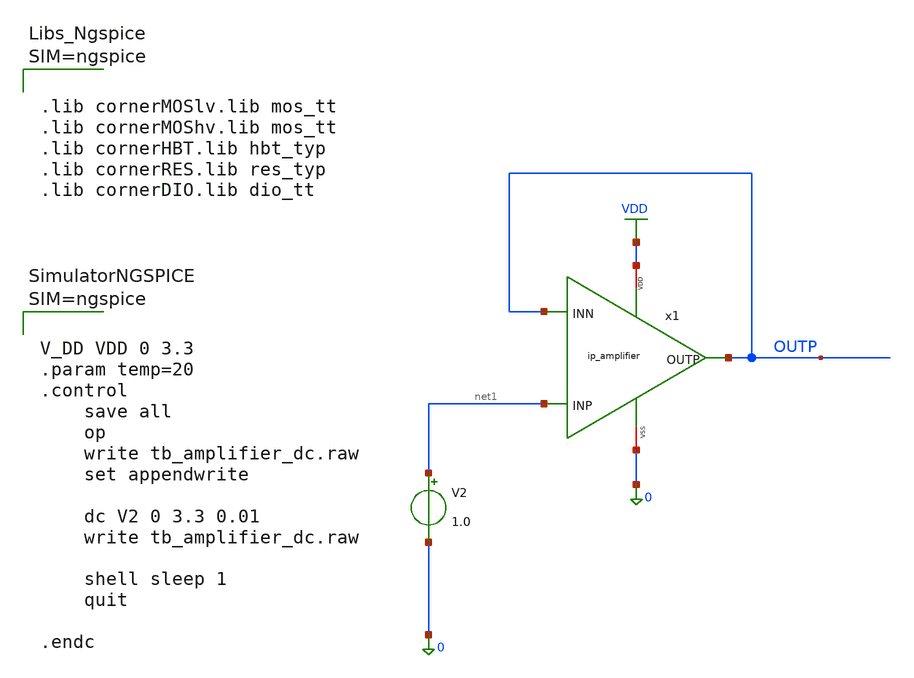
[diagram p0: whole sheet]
** sch_path: xschem/tb_amplifier_dc.sch
**.subckt tb_amplifier_dc
x1 VDD OUTP OUTP net1 0 ip_amplifier
V2 net1 0 1.0
**** begin user architecture code



.lib cornerMOSlv.lib mos_tt
.lib cornerMOShv.lib mos_tt
.lib cornerHBT.lib hbt_typ
.lib cornerRES.lib res_typ
.lib cornerDIO.lib dio_tt






V_DD VDD 0 3.3
.param temp=20
.control
	save all
	op
	write tb_amplifier_dc.raw
	set appendwrite

	dc V2 0 3.3 0.01
	write tb_amplifier_dc.raw

	shell sleep 1
	quit

.endc



**** end user architecture code
**.ends

* expanding   symbol:  ip_amplifier.sym # of pins=5
** sym_path: xschem/ip_amplifier.sym
** sch_path: xschem/ip_amplifier.sch
.subckt ip_amplifier VDD OUTP INN INP VSS
*.iopin VSS
*.iopin VDD
*.opin OUTP
*.ipin INN
*.ipin INP
XM1 net2 BIAS_N VSS VSS sg13_hv_nmos w=10u l=5u ng=1 m=1 mm_ok=1
R1 VDD net8 30k m=2
XM2 net1 BIAS_N VSS VSS sg13_hv_nmos w=10u l=5u ng=1 m=1 mm_ok=1
XM3 net5 BIAS_N net1 VSS sg13_hv_nmos w=10u l=0.5u ng=1 m=20 mm_ok=1
XM4 BIAS_N BIAS_N net2 VSS sg13_hv_nmos w=10u l=0.5u ng=1 m=20 mm_ok=1
Vmeas BIAS_P net5 0
Vmeas1 net6 net7 0
XM5 net6 BIAS_P net4 VDD sg13_hv_pmos w=10u l=0.5u ng=1 m=30 mm_ok=1
XM6 net4 BIAS_P VDD VDD sg13_hv_pmos w=10u l=5u ng=1 m=2 mm_ok=1
XM7 net3 BIAS_P VDD VDD sg13_hv_pmos w=10u l=5u ng=1 m=2 mm_ok=1
XM8 BIAS_P BIAS_P net3 VDD sg13_hv_pmos w=10u l=0.5u ng=1 m=30 mm_ok=1
Vmeas2 net8 BIAS_N 0
XM9 COMP INP net7 VDD sg13_hv_pmos w=10u l=5u ng=1 m=20 mm_ok=1
XM10 net9 INN net7 VDD sg13_hv_pmos w=10u l=5u ng=1 m=20 mm_ok=1
XM11 net9 net9 VSS VSS sg13_hv_nmos w=10u l=5u ng=1 m=10 mm_ok=1
XM12 COMP net9 VSS VSS sg13_hv_nmos w=10u l=5u ng=1 m=10 mm_ok=1
XM13 net10 BIAS_P VDD VDD sg13_hv_pmos w=10u l=0.5u ng=1 m=5 mm_ok=1
XM14 OUTP COMP VSS VSS sg13_hv_nmos w=10u l=0.5u ng=1 m=10 mm_ok=1
Vmeas3 net10 OUTP 0
.ends

.GLOBAL VDD
.end
